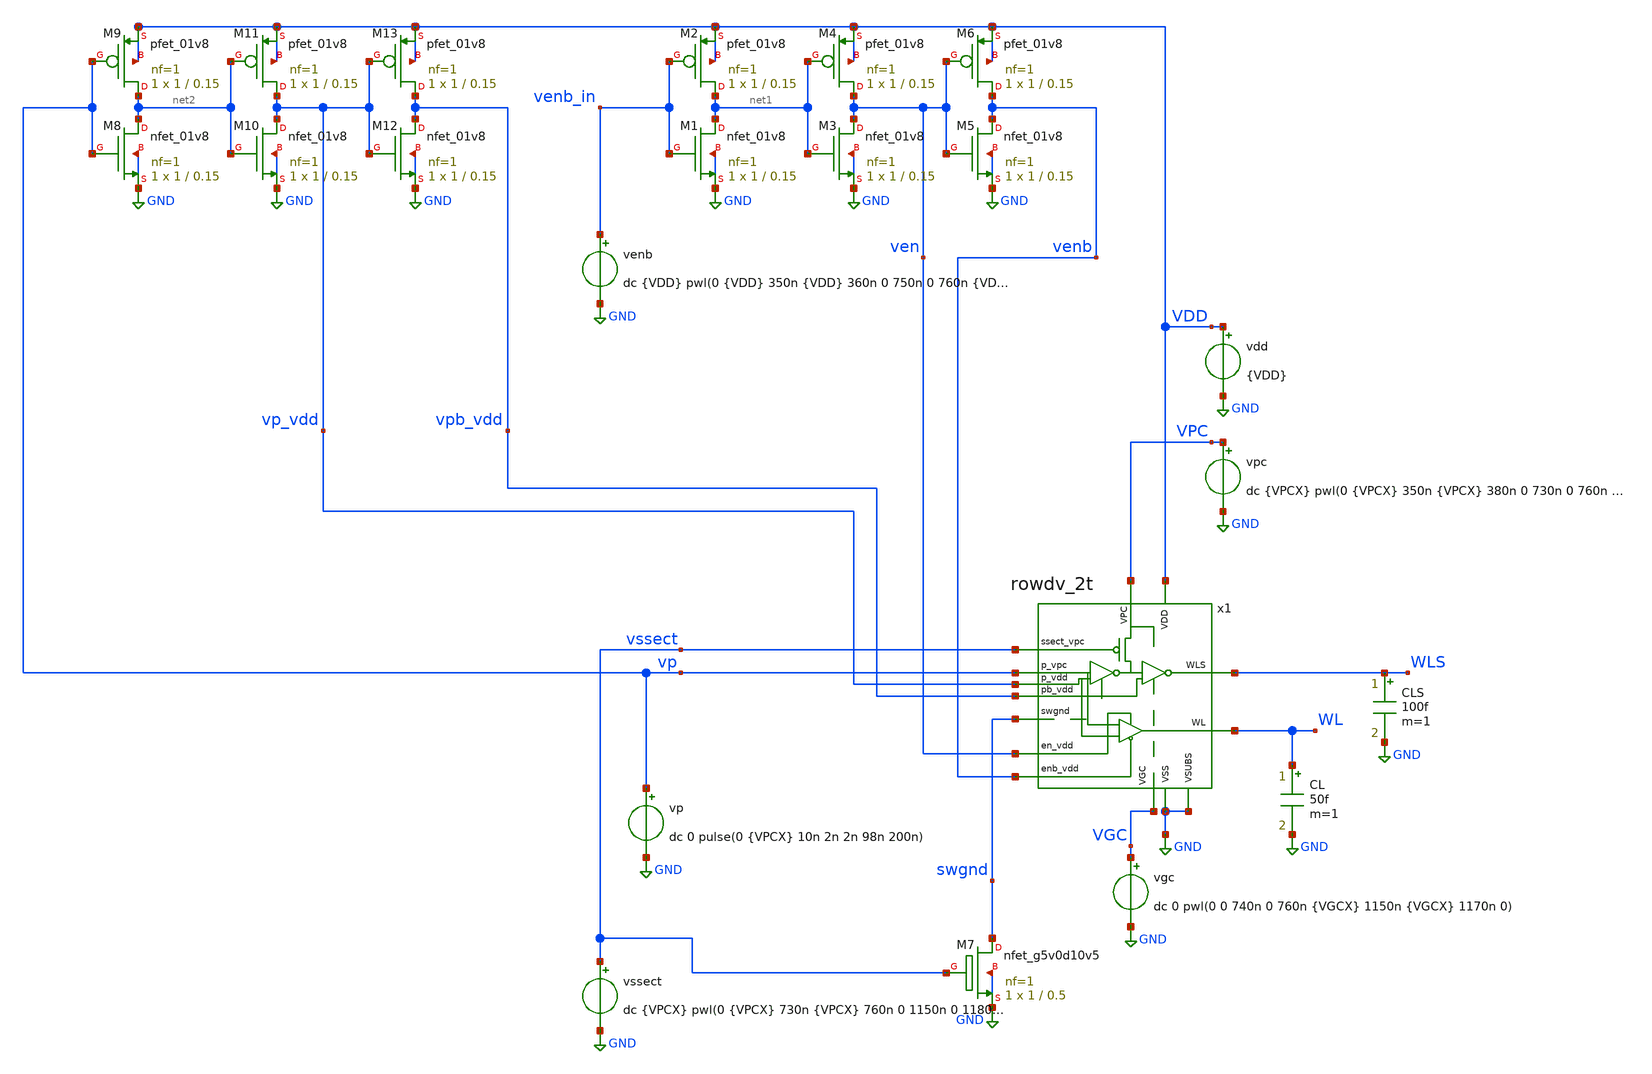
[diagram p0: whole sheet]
** sch_path: row_drivers/test_rowdv_2t.sch
**.subckt test_rowdv_2t
vssect vssect GND dc {VPCX} pwl(0 {VPCX} 730n {VPCX} 760n 0 1150n 0 1180n {VPCX})
vp vp GND dc 0 pulse(0 {VPCX} 10n 2n 2n 98n 200n)
venb venb_in GND dc {VDD} pwl(0 {VDD} 350n {VDD} 360n 0 750n 0 760n {VDD} 1170n {VDD} 1180n 0)
XM1 net1 venb_in GND GND sky130_fd_pr__nfet_01v8 L=0.15 W=1 nf=1 ad='int((nf+1)/2) * W/nf * 0.29' as='int((nf+2)/2) * W/nf * 0.29'
+ pd='2*int((nf+1)/2) * (W/nf + 0.29)' ps='2*int((nf+2)/2) * (W/nf + 0.29)' nrd='0.29 / W' nrs='0.29 / W'
+ sa=0 sb=0 sd=0 mult=1 m=1
XM2 net1 venb_in VDD VDD sky130_fd_pr__pfet_01v8 L=0.15 W=1 nf=1 ad='int((nf+1)/2) * W/nf * 0.29' as='int((nf+2)/2) * W/nf * 0.29'
+ pd='2*int((nf+1)/2) * (W/nf + 0.29)' ps='2*int((nf+2)/2) * (W/nf + 0.29)' nrd='0.29 / W' nrs='0.29 / W'
+ sa=0 sb=0 sd=0 mult=1 m=1
vpc VPC GND dc {VPCX} pwl(0 {VPCX} 350n {VPCX} 380n 0 730n 0 760n {VDD} 1140n {VDD} 1170n 0)
vdd VDD GND {VDD}
vgc VGC GND dc 0 pwl(0 0 740n 0 760n {VGCX} 1150n {VGCX} 1170n 0)
XM3 ven net1 GND GND sky130_fd_pr__nfet_01v8 L=0.15 W=1 nf=1 ad='int((nf+1)/2) * W/nf * 0.29' as='int((nf+2)/2) * W/nf * 0.29'
+ pd='2*int((nf+1)/2) * (W/nf + 0.29)' ps='2*int((nf+2)/2) * (W/nf + 0.29)' nrd='0.29 / W' nrs='0.29 / W'
+ sa=0 sb=0 sd=0 mult=1 m=1
XM4 ven net1 VDD VDD sky130_fd_pr__pfet_01v8 L=0.15 W=1 nf=1 ad='int((nf+1)/2) * W/nf * 0.29' as='int((nf+2)/2) * W/nf * 0.29'
+ pd='2*int((nf+1)/2) * (W/nf + 0.29)' ps='2*int((nf+2)/2) * (W/nf + 0.29)' nrd='0.29 / W' nrs='0.29 / W'
+ sa=0 sb=0 sd=0 mult=1 m=1
XM5 venb ven GND GND sky130_fd_pr__nfet_01v8 L=0.15 W=1 nf=1 ad='int((nf+1)/2) * W/nf * 0.29' as='int((nf+2)/2) * W/nf * 0.29'
+ pd='2*int((nf+1)/2) * (W/nf + 0.29)' ps='2*int((nf+2)/2) * (W/nf + 0.29)' nrd='0.29 / W' nrs='0.29 / W'
+ sa=0 sb=0 sd=0 mult=1 m=1
XM6 venb ven VDD VDD sky130_fd_pr__pfet_01v8 L=0.15 W=1 nf=1 ad='int((nf+1)/2) * W/nf * 0.29' as='int((nf+2)/2) * W/nf * 0.29'
+ pd='2*int((nf+1)/2) * (W/nf + 0.29)' ps='2*int((nf+2)/2) * (W/nf + 0.29)' nrd='0.29 / W' nrs='0.29 / W'
+ sa=0 sb=0 sd=0 mult=1 m=1
CLS WLS GND 100f m=1
CL WL GND 50f m=1
XM7 swgnd vssect GND GND sky130_fd_pr__nfet_g5v0d10v5 L=0.5 W=1 nf=1 ad='int((nf+1)/2) * W/nf * 0.29'
+ as='int((nf+2)/2) * W/nf * 0.29' pd='2*int((nf+1)/2) * (W/nf + 0.29)' ps='2*int((nf+2)/2) * (W/nf + 0.29)'
+ nrd='0.29 / W' nrs='0.29 / W' sa=0 sb=0 sd=0 mult=1 m=1
x1 vssect ven venb vp vp_vdd vpb_vdd swgnd VPC VGC VDD GND GND WLS WL rowdv_2t
XM8 net2 vp GND GND sky130_fd_pr__nfet_01v8 L=0.15 W=1 nf=1 ad='int((nf+1)/2) * W/nf * 0.29' as='int((nf+2)/2) * W/nf * 0.29'
+ pd='2*int((nf+1)/2) * (W/nf + 0.29)' ps='2*int((nf+2)/2) * (W/nf + 0.29)' nrd='0.29 / W' nrs='0.29 / W'
+ sa=0 sb=0 sd=0 mult=1 m=1
XM9 net2 vp VDD VDD sky130_fd_pr__pfet_01v8 L=0.15 W=1 nf=1 ad='int((nf+1)/2) * W/nf * 0.29' as='int((nf+2)/2) * W/nf * 0.29'
+ pd='2*int((nf+1)/2) * (W/nf + 0.29)' ps='2*int((nf+2)/2) * (W/nf + 0.29)' nrd='0.29 / W' nrs='0.29 / W'
+ sa=0 sb=0 sd=0 mult=1 m=1
XM10 vp_vdd net2 GND GND sky130_fd_pr__nfet_01v8 L=0.15 W=1 nf=1 ad='int((nf+1)/2) * W/nf * 0.29' as='int((nf+2)/2) * W/nf * 0.29'
+ pd='2*int((nf+1)/2) * (W/nf + 0.29)' ps='2*int((nf+2)/2) * (W/nf + 0.29)' nrd='0.29 / W' nrs='0.29 / W'
+ sa=0 sb=0 sd=0 mult=1 m=1
XM11 vp_vdd net2 VDD VDD sky130_fd_pr__pfet_01v8 L=0.15 W=1 nf=1 ad='int((nf+1)/2) * W/nf * 0.29' as='int((nf+2)/2) * W/nf * 0.29'
+ pd='2*int((nf+1)/2) * (W/nf + 0.29)' ps='2*int((nf+2)/2) * (W/nf + 0.29)' nrd='0.29 / W' nrs='0.29 / W'
+ sa=0 sb=0 sd=0 mult=1 m=1
XM12 vpb_vdd vp_vdd GND GND sky130_fd_pr__nfet_01v8 L=0.15 W=1 nf=1 ad='int((nf+1)/2) * W/nf * 0.29'
+ as='int((nf+2)/2) * W/nf * 0.29' pd='2*int((nf+1)/2) * (W/nf + 0.29)' ps='2*int((nf+2)/2) * (W/nf + 0.29)'
+ nrd='0.29 / W' nrs='0.29 / W' sa=0 sb=0 sd=0 mult=1 m=1
XM13 vpb_vdd vp_vdd VDD VDD sky130_fd_pr__pfet_01v8 L=0.15 W=1 nf=1 ad='int((nf+1)/2) * W/nf * 0.29'
+ as='int((nf+2)/2) * W/nf * 0.29' pd='2*int((nf+1)/2) * (W/nf + 0.29)' ps='2*int((nf+2)/2) * (W/nf + 0.29)'
+ nrd='0.29 / W' nrs='0.29 / W' sa=0 sb=0 sd=0 mult=1 m=1
**** begin user architecture code

** opencircuitdesign pdks install
.lib $::SKYWATER_MODELS/sky130.lib.spice tt




.param VDD=1.8
.param VPCX=6.7
.param VGCX=-3.8
.option savecurrents
.control
  unset appendwrite
  save all
  op
  remzerovec
  write test_rowdv_2t.raw
  *set appendwrite

  tran 1n 1.6u
  remzerovec
  write test_rowdv_2t.raw
.endc


**** end user architecture code
**.ends

* expanding   symbol:  rowdv_2t.sym # of pins=14
** sym_path: integrated/rowdv_2t_sonos/rowdv_2t.sym
** sch_path: integrated/rowdv_2t_sonos/rowdv_2t.sch
.subckt rowdv_2t ssect_vpc en_vdd enb_vdd p_vpc p_vdd pb_vdd swgnd VPC VGC VDD VSS VSUBS WLS WL
*.ipin p_vpc
*.opin WLS
*.ipin swgnd
*.ipin VDD
*.ipin VSS
*.ipin en_vdd
*.ipin enb_vdd
*.ipin VGC
*.ipin VPC
*.ipin ssect_vpc
*.opin WL
*.ipin VSUBS
*.ipin p_vdd
*.ipin pb_vdd
XM1 wlsx p_vdd swgnd VSUBS sky130_fd_pr__nfet_g5v0d10v5 L=0.5 W=1 nf=1 ad='int((nf+1)/2) * W/nf * 0.29'
+ as='int((nf+2)/2) * W/nf * 0.29' pd='2*int((nf+1)/2) * (W/nf + 0.29)' ps='2*int((nf+2)/2) * (W/nf + 0.29)'
+ nrd='0.29 / W' nrs='0.29 / W' sa=0 sb=0 sd=0 mult=1 m=1
XM2 pbs p_vpc VPC VPC sky130_fd_pr__pfet_g5v0d10v5 L=0.5 W=1 nf=1 ad='int((nf+1)/2) * W/nf * 0.29' as='int((nf+2)/2) * W/nf * 0.29'
+ pd='2*int((nf+1)/2) * (W/nf + 0.29)' ps='2*int((nf+2)/2) * (W/nf + 0.29)' nrd='0.29 / W' nrs='0.29 / W'
+ sa=0 sb=0 sd=0 mult=1 m=1
XM3 wlsy pb_vdd VGC VGC sky130_fd_pr__nfet_g5v0d10v5 L=0.5 W=5 nf=1 ad='int((nf+1)/2) * W/nf * 0.29'
+ as='int((nf+2)/2) * W/nf * 0.29' pd='2*int((nf+1)/2) * (W/nf + 0.29)' ps='2*int((nf+2)/2) * (W/nf + 0.29)'
+ nrd='0.29 / W' nrs='0.29 / W' sa=0 sb=0 sd=0 mult=1 m=1
XM4 WLS pbs VPC VPC sky130_fd_pr__pfet_g5v0d10v5 L=0.5 W=5 nf=1 ad='int((nf+1)/2) * W/nf * 0.29' as='int((nf+2)/2) * W/nf * 0.29'
+ pd='2*int((nf+1)/2) * (W/nf + 0.29)' ps='2*int((nf+2)/2) * (W/nf + 0.29)' nrd='0.29 / W' nrs='0.29 / W'
+ sa=0 sb=0 sd=0 mult=1 m=1
XM6 pbpass p_vpc VDD VDD sky130_fd_pr__pfet_g5v0d10v5 L=0.5 W=1 nf=1 ad='int((nf+1)/2) * W/nf * 0.29'
+ as='int((nf+2)/2) * W/nf * 0.29' pd='2*int((nf+1)/2) * (W/nf + 0.29)' ps='2*int((nf+2)/2) * (W/nf + 0.29)'
+ nrd='0.29 / W' nrs='0.29 / W' sa=0 sb=0 sd=0 mult=1 m=1
XM7 wlil pbpass VSS VSUBS sky130_fd_pr__nfet_g5v0d10v5 L=0.5 W=5 nf=1 ad='int((nf+1)/2) * W/nf * 0.29'
+ as='int((nf+2)/2) * W/nf * 0.29' pd='2*int((nf+1)/2) * (W/nf + 0.29)' ps='2*int((nf+2)/2) * (W/nf + 0.29)'
+ nrd='0.29 / W' nrs='0.29 / W' sa=0 sb=0 sd=0 mult=1 m=1
XM9 WL en_vdd wlih VDD sky130_fd_pr__pfet_g5v0d10v5 L=0.5 W=10 nf=1 ad='int((nf+1)/2) * W/nf * 0.29'
+ as='int((nf+2)/2) * W/nf * 0.29' pd='2*int((nf+1)/2) * (W/nf + 0.29)' ps='2*int((nf+2)/2) * (W/nf + 0.29)'
+ nrd='0.29 / W' nrs='0.29 / W' sa=0 sb=0 sd=0 mult=1 m=1
XM8 WL enb_vdd wlil VSUBS sky130_fd_pr__nfet_g5v0d10v5 L=0.5 W=5 nf=1 ad='int((nf+1)/2) * W/nf * 0.29'
+ as='int((nf+2)/2) * W/nf * 0.29' pd='2*int((nf+1)/2) * (W/nf + 0.29)' ps='2*int((nf+2)/2) * (W/nf + 0.29)'
+ nrd='0.29 / W' nrs='0.29 / W' sa=0 sb=0 sd=0 mult=1 m=1
XM10 wlih pbpass VDD VDD sky130_fd_pr__pfet_g5v0d10v5 L=0.5 W=10 nf=1 ad='int((nf+1)/2) * W/nf * 0.29'
+ as='int((nf+2)/2) * W/nf * 0.29' pd='2*int((nf+1)/2) * (W/nf + 0.29)' ps='2*int((nf+2)/2) * (W/nf + 0.29)'
+ nrd='0.29 / W' nrs='0.29 / W' sa=0 sb=0 sd=0 mult=1 m=1
XM11 pbs ssect_vpc VPC VPC sky130_fd_pr__pfet_g5v0d10v5 L=0.5 W=1 nf=1 ad='int((nf+1)/2) * W/nf * 0.29'
+ as='int((nf+2)/2) * W/nf * 0.29' pd='2*int((nf+1)/2) * (W/nf + 0.29)' ps='2*int((nf+2)/2) * (W/nf + 0.29)'
+ nrd='0.29 / W' nrs='0.29 / W' sa=0 sb=0 sd=0 mult=1 m=1
XM5 pbpass p_vdd VSS VSS sky130_fd_pr__nfet_g5v0d10v5 L=0.5 W=1 nf=1 ad='int((nf+1)/2) * W/nf * 0.29'
+ as='int((nf+2)/2) * W/nf * 0.29' pd='2*int((nf+1)/2) * (W/nf + 0.29)' ps='2*int((nf+2)/2) * (W/nf + 0.29)'
+ nrd='0.29 / W' nrs='0.29 / W' sa=0 sb=0 sd=0 mult=1 m=1
XM1x pbs VDD wlsx VSUBS sky130_fd_pr__nfet_g5v0d10v5 L=0.5 W=1 nf=1 ad='int((nf+1)/2) * W/nf * 0.29'
+ as='int((nf+2)/2) * W/nf * 0.29' pd='2*int((nf+1)/2) * (W/nf + 0.29)' ps='2*int((nf+2)/2) * (W/nf + 0.29)'
+ nrd='0.29 / W' nrs='0.29 / W' sa=0 sb=0 sd=0 mult=1 m=1
XM3x WLS VDD wlsy VGC sky130_fd_pr__nfet_g5v0d10v5 L=0.5 W=5 nf=1 ad='int((nf+1)/2) * W/nf * 0.29' as='int((nf+2)/2) * W/nf * 0.29'
+ pd='2*int((nf+1)/2) * (W/nf + 0.29)' ps='2*int((nf+2)/2) * (W/nf + 0.29)' nrd='0.29 / W' nrs='0.29 / W'
+ sa=0 sb=0 sd=0 mult=1 m=1
.ends

.GLOBAL GND
.end
